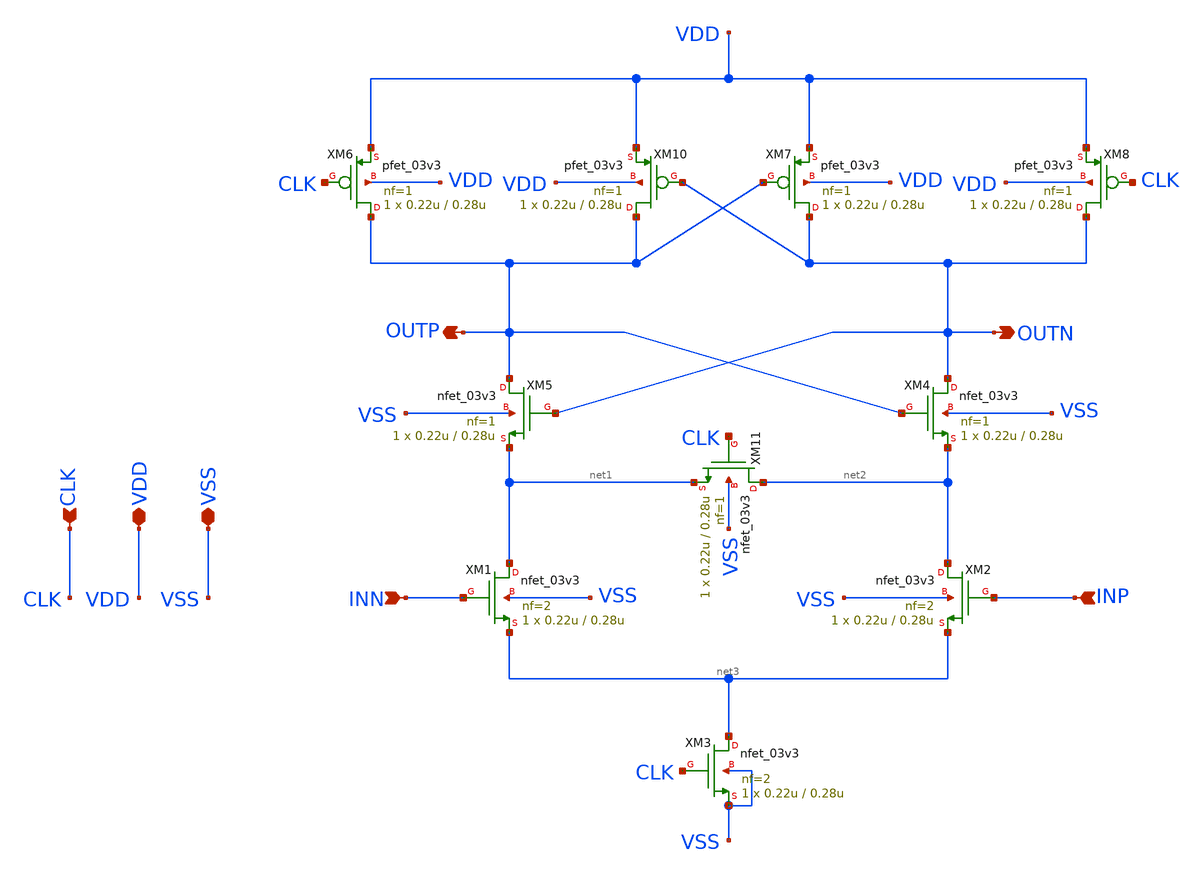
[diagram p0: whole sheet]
** sch_path: analog/blocks/Double_Tail_Comparator/funkercomp.sch
**.subckt funkercomp CLK VSS VDD OUTP OUTN INN INP
*.ipin CLK
*.iopin VSS
*.iopin VDD
*.opin OUTP
*.opin OUTN
*.ipin INN
*.ipin INP
XM1 net1 INN net3 VSS nfet_03v3 L=0.28u W=0.22u nf=2 ad='int((nf+1)/2) * W/nf * 0.18u' as='int((nf+2)/2) * W/nf * 0.18u'
+ pd='2*int((nf+1)/2) * (W/nf + 0.18u)' ps='2*int((nf+2)/2) * (W/nf + 0.18u)' nrd='0.18u / W' nrs='0.18u / W'
+ sa=0 sb=0 sd=0 m=1
XM2 net2 INP net3 VSS nfet_03v3 L=0.28u W=0.22u nf=2 ad='int((nf+1)/2) * W/nf * 0.18u' as='int((nf+2)/2) * W/nf * 0.18u'
+ pd='2*int((nf+1)/2) * (W/nf + 0.18u)' ps='2*int((nf+2)/2) * (W/nf + 0.18u)' nrd='0.18u / W' nrs='0.18u / W'
+ sa=0 sb=0 sd=0 m=1
XM3 net3 CLK VSS VSS nfet_03v3 L=0.28u W=0.22u nf=2 ad='int((nf+1)/2) * W/nf * 0.18u' as='int((nf+2)/2) * W/nf * 0.18u'
+ pd='2*int((nf+1)/2) * (W/nf + 0.18u)' ps='2*int((nf+2)/2) * (W/nf + 0.18u)' nrd='0.18u / W' nrs='0.18u / W'
+ sa=0 sb=0 sd=0 m=1
XM4 OUTN OUTP net2 VSS nfet_03v3 L=0.28u W=0.22u nf=1 ad='int((nf+1)/2) * W/nf * 0.18u' as='int((nf+2)/2) * W/nf * 0.18u'
+ pd='2*int((nf+1)/2) * (W/nf + 0.18u)' ps='2*int((nf+2)/2) * (W/nf + 0.18u)' nrd='0.18u / W' nrs='0.18u / W'
+ sa=0 sb=0 sd=0 m=1
XM5 OUTP OUTN net1 VSS nfet_03v3 L=0.28u W=0.22u nf=1 ad='int((nf+1)/2) * W/nf * 0.18u' as='int((nf+2)/2) * W/nf * 0.18u'
+ pd='2*int((nf+1)/2) * (W/nf + 0.18u)' ps='2*int((nf+2)/2) * (W/nf + 0.18u)' nrd='0.18u / W' nrs='0.18u / W'
+ sa=0 sb=0 sd=0 m=1
XM6 OUTP CLK VDD VDD pfet_03v3 L=0.28u W=0.22u nf=1 ad='int((nf+1)/2) * W/nf * 0.18u' as='int((nf+2)/2) * W/nf * 0.18u'
+ pd='2*int((nf+1)/2) * (W/nf + 0.18u)' ps='2*int((nf+2)/2) * (W/nf + 0.18u)' nrd='0.18u / W' nrs='0.18u / W'
+ sa=0 sb=0 sd=0 m=1
XM7 OUTN OUTP VDD VDD pfet_03v3 L=0.28u W=0.22u nf=1 ad='int((nf+1)/2) * W/nf * 0.18u' as='int((nf+2)/2) * W/nf * 0.18u'
+ pd='2*int((nf+1)/2) * (W/nf + 0.18u)' ps='2*int((nf+2)/2) * (W/nf + 0.18u)' nrd='0.18u / W' nrs='0.18u / W'
+ sa=0 sb=0 sd=0 m=1
XM8 OUTN CLK VDD VDD pfet_03v3 L=0.28u W=0.22u nf=1 ad='int((nf+1)/2) * W/nf * 0.18u' as='int((nf+2)/2) * W/nf * 0.18u'
+ pd='2*int((nf+1)/2) * (W/nf + 0.18u)' ps='2*int((nf+2)/2) * (W/nf + 0.18u)' nrd='0.18u / W' nrs='0.18u / W'
+ sa=0 sb=0 sd=0 m=1
XM10 OUTP OUTN VDD VDD pfet_03v3 L=0.28u W=0.22u nf=1 ad='int((nf+1)/2) * W/nf * 0.18u' as='int((nf+2)/2) * W/nf * 0.18u'
+ pd='2*int((nf+1)/2) * (W/nf + 0.18u)' ps='2*int((nf+2)/2) * (W/nf + 0.18u)' nrd='0.18u / W' nrs='0.18u / W'
+ sa=0 sb=0 sd=0 m=1
XM11 net2 CLK net1 VSS nfet_03v3 L=0.28u W=0.22u nf=1 ad='int((nf+1)/2) * W/nf * 0.18u' as='int((nf+2)/2) * W/nf * 0.18u'
+ pd='2*int((nf+1)/2) * (W/nf + 0.18u)' ps='2*int((nf+2)/2) * (W/nf + 0.18u)' nrd='0.18u / W' nrs='0.18u / W'
+ sa=0 sb=0 sd=0 m=1
**.ends
.end
